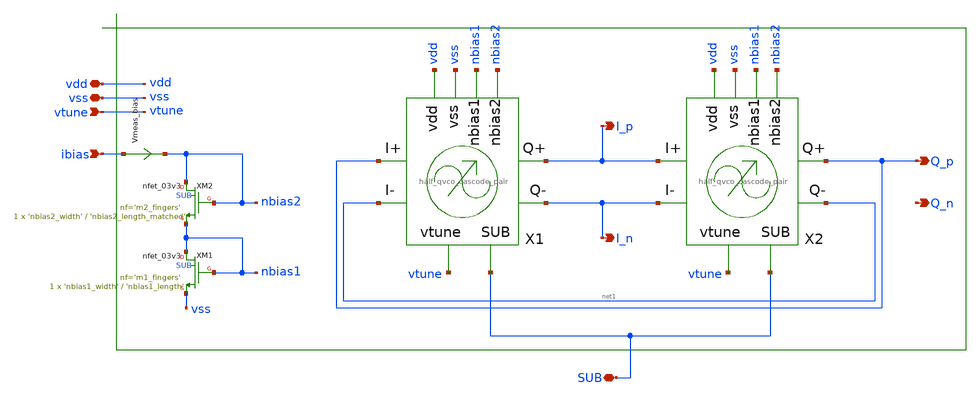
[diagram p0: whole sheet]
** sch_path: sch/vco/vco_quadrature_lc_cascode1.sch
**.subckt vco_quadrature_lc_cascode1 vdd vss vtune I_p I_n Q_p Q_n ibias SUB
*.iopin vdd
*.iopin vss
*.ipin vtune
*.opin I_p
*.opin I_n
*.opin Q_p
*.opin Q_n
*.ipin ibias
*.iopin SUB
XM1 nbias1 nbias1 vss SUB nfet_03v3 L='nbias1_length' W='nbias1_width' nf='m1_fingers' ad='int((nf+1)/2) * W/nf * 0.18u'
+ as='int((nf+2)/2) * W/nf * 0.18u' pd='2*int((nf+1)/2) * (W/nf + 0.18u)' ps='2*int((nf+2)/2) * (W/nf + 0.18u)'
+ nrd='0.18u / W' nrs='0.18u / W' sa=0 sb=0 sd=0 m=1 par=1
XM2 nbias2 nbias2 nbias1 SUB nfet_03v3 L='nbias2_length_matched' W='nbias2_width' nf='m2_fingers' ad='int((nf+1)/2) * W/nf * 0.18u'
+ as='int((nf+2)/2) * W/nf * 0.18u' pd='2*int((nf+1)/2) * (W/nf + 0.18u)' ps='2*int((nf+2)/2) * (W/nf + 0.18u)'
+ nrd='0.18u / W' nrs='0.18u / W' sa=0 sb=0 sd=0 m=1 par=1
X1 vdd vss nbias1 Q_p net1 I_p I_n vtune SUB nbias2 half_qvco_cascode_pair m1m2_width='m1m2_width' m1m2_length='m1m2_length'
+ m1m2_fingers='m1m2_fingers' m1m2_mult='m1m2_mult' m3m4_width='m3m4_width' m3m4_length='m3m4_length' m3m4_fingers='m3m4_fingers'
+ m3m4_mult='m3m4_mult' m5_width='m5_width_matched' m5_length='m5_length_matched' m5_fingers='m5_fingers'
+ m5_mult='m5_mult' m6m7_width='m6m7_width' m6m7_length='m6m7_length' m6m7_fingers='m6m7_fingers' m6m7_mult='m6m7_mult'
+ capvar_width='capvar_width' capvar_length='capvar_length' capvar_mult='capvar_mult'
X2 vdd vss nbias1 I_p I_n Q_p net1 vtune SUB nbias2 half_qvco_cascode_pair m1m2_width='m1m2_width' m1m2_length='m1m2_length'
+ m1m2_fingers='m1m2_fingers' m1m2_mult='m1m2_mult' m3m4_width='m3m4_width' m3m4_length='m3m4_length' m3m4_fingers='m3m4_fingers'
+ m3m4_mult='m3m4_mult' m5_width='m5_width_matched' m5_length='m5_length_matched' m5_fingers='m5_fingers'
+ m5_mult='m5_mult' m6m7_width='m6m7_width' m6m7_length='m6m7_length' m6m7_fingers='m6m7_fingers' m6m7_mult='m6m7_mult'
+ capvar_width='capvar_width' capvar_length='capvar_length' capvar_mult='capvar_mult'
Vmeas_bias ibias nbias2 0
.save i(vmeas_bias)
**.ends
.end
